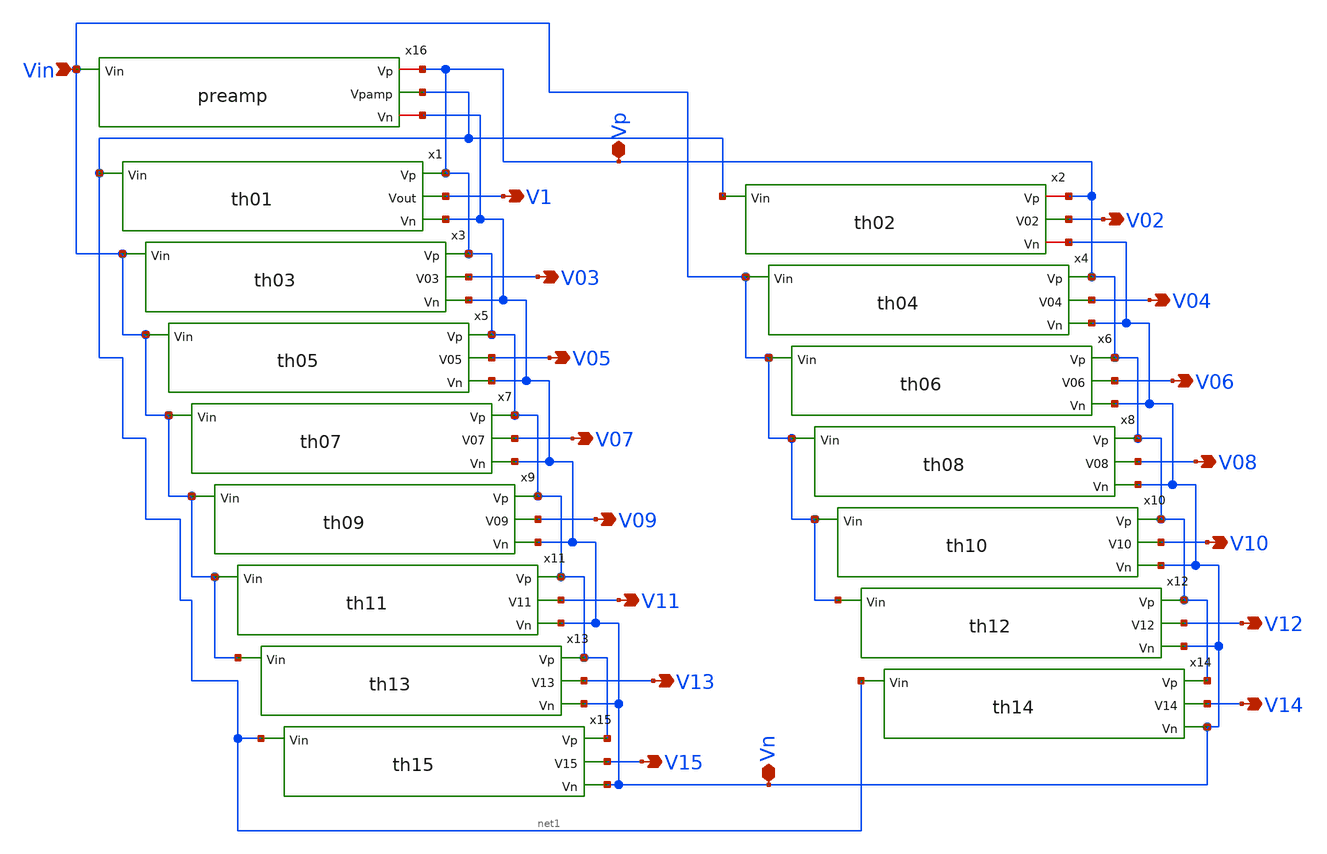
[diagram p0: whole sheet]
** sch_path: xschem/Vth_sch/Symbol/Analog2.sch
**.subckt Analog2 Vin Vp Vn V10 V12 V14 V15 V1 V11 V13 V09 V07 V05 V03 V02 V04 V06 V08
*.ipin Vin
*.iopin Vp
*.iopin Vn
*.opin V10
*.opin V12
*.opin V14
*.opin V15
*.opin V1
*.opin V11
*.opin V13
*.opin V09
*.opin V07
*.opin V05
*.opin V03
*.opin V02
*.opin V04
*.opin V06
*.opin V08
x1 Vp net1 V1 Vn th01
x2 Vp net1 V02 Vn th02
x3 Vp V03 Vin Vn th03
x4 Vp V04 Vin Vn th04
x5 Vp V05 Vin Vn th05
x6 Vp Vin V06 Vn th06
x7 Vp Vin V07 Vn th07
x8 Vp V08 Vin Vn th08
x9 Vp V09 Vin Vn th09
x10 Vp V10 Vin Vn th10
x11 Vp V11 Vin Vn th11
x12 Vp V12 Vin Vn th12
x13 Vp V13 Vin Vn th13
x14 Vp V14 net1 Vn th14
x15 Vp V15 net1 Vn th15
x16 Vp Vin net1 Vn preamp
**.ends
.end
